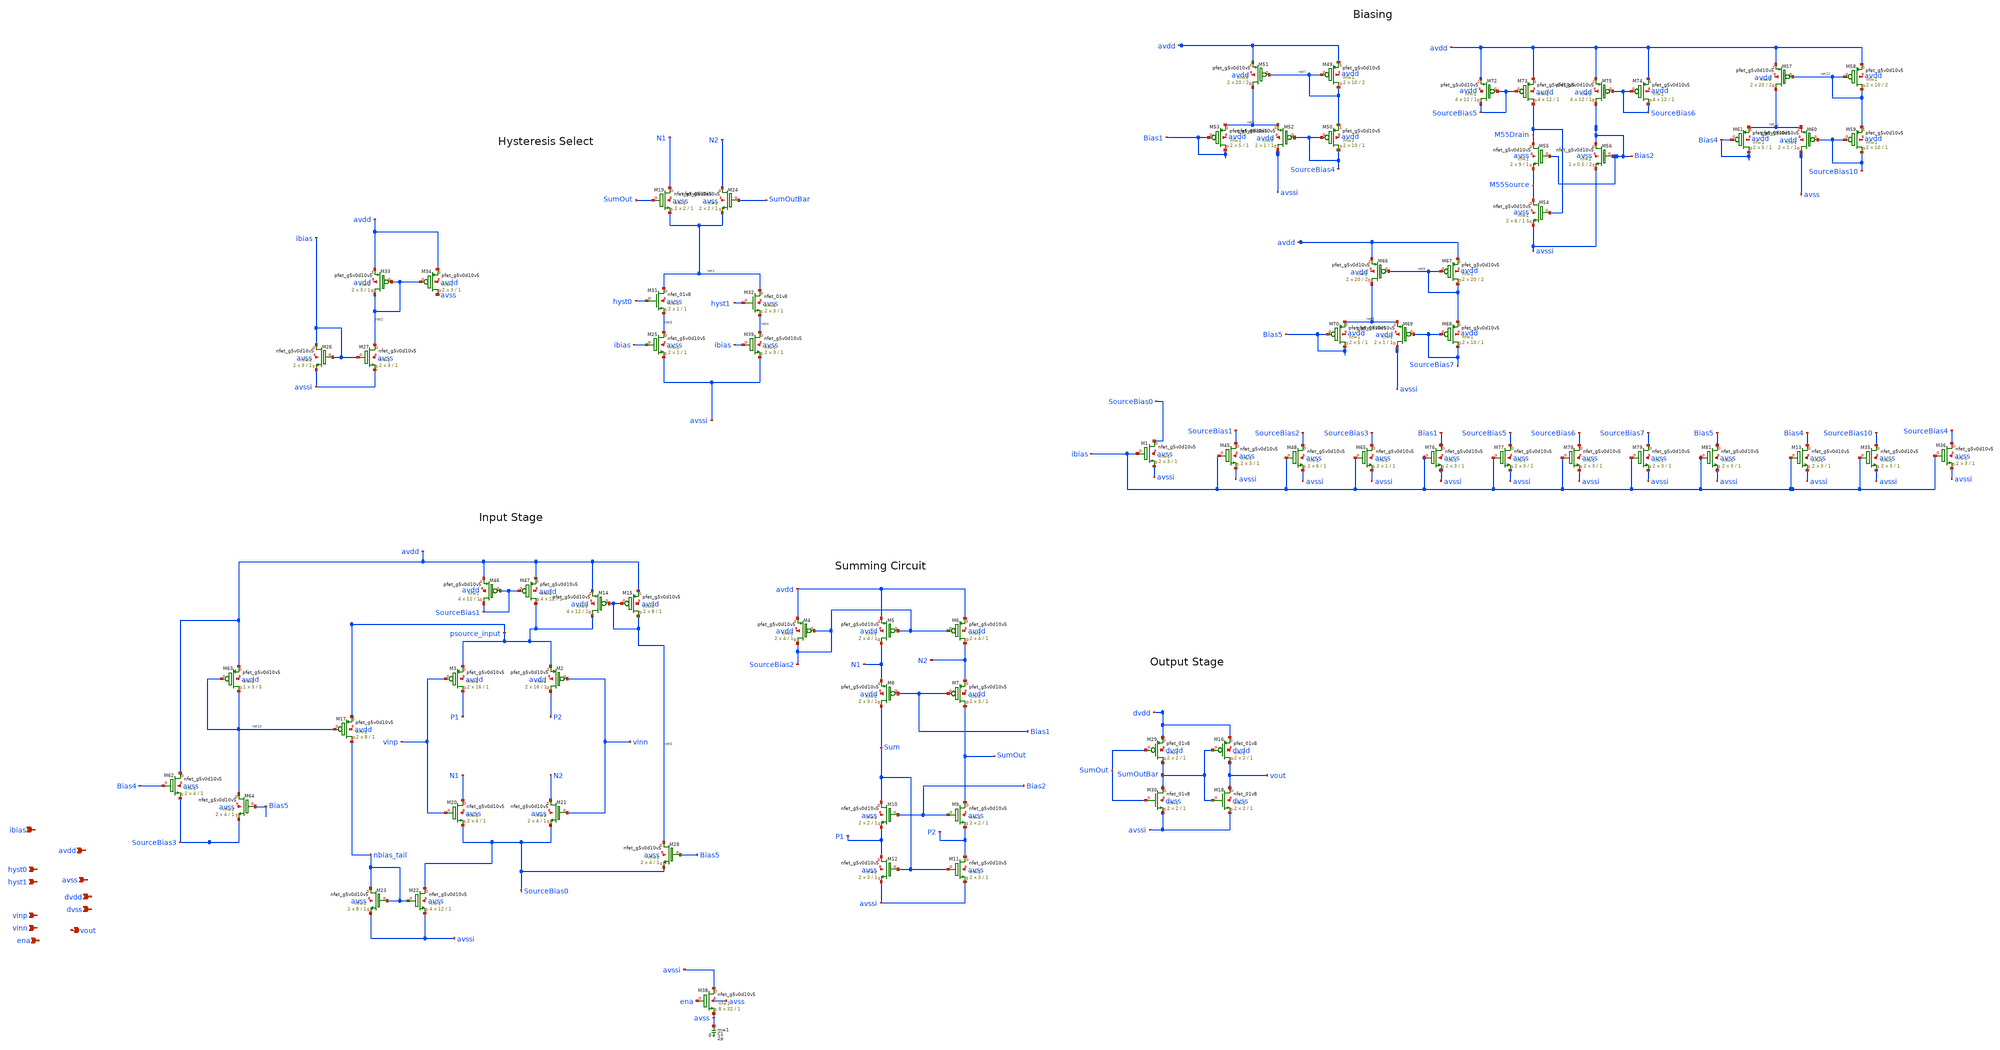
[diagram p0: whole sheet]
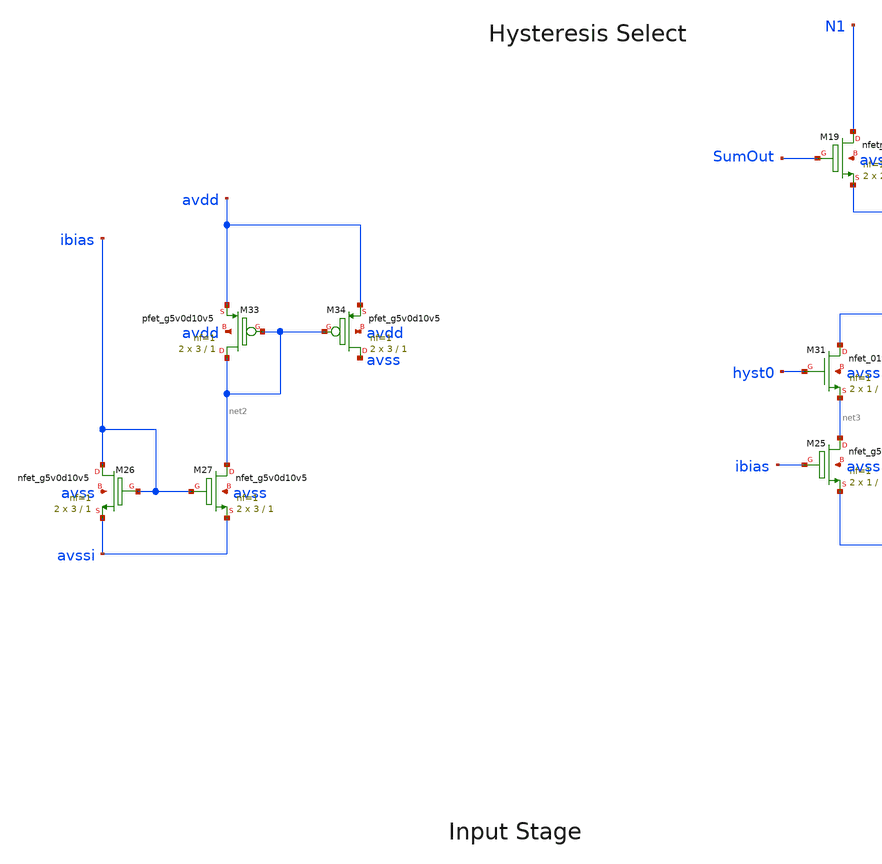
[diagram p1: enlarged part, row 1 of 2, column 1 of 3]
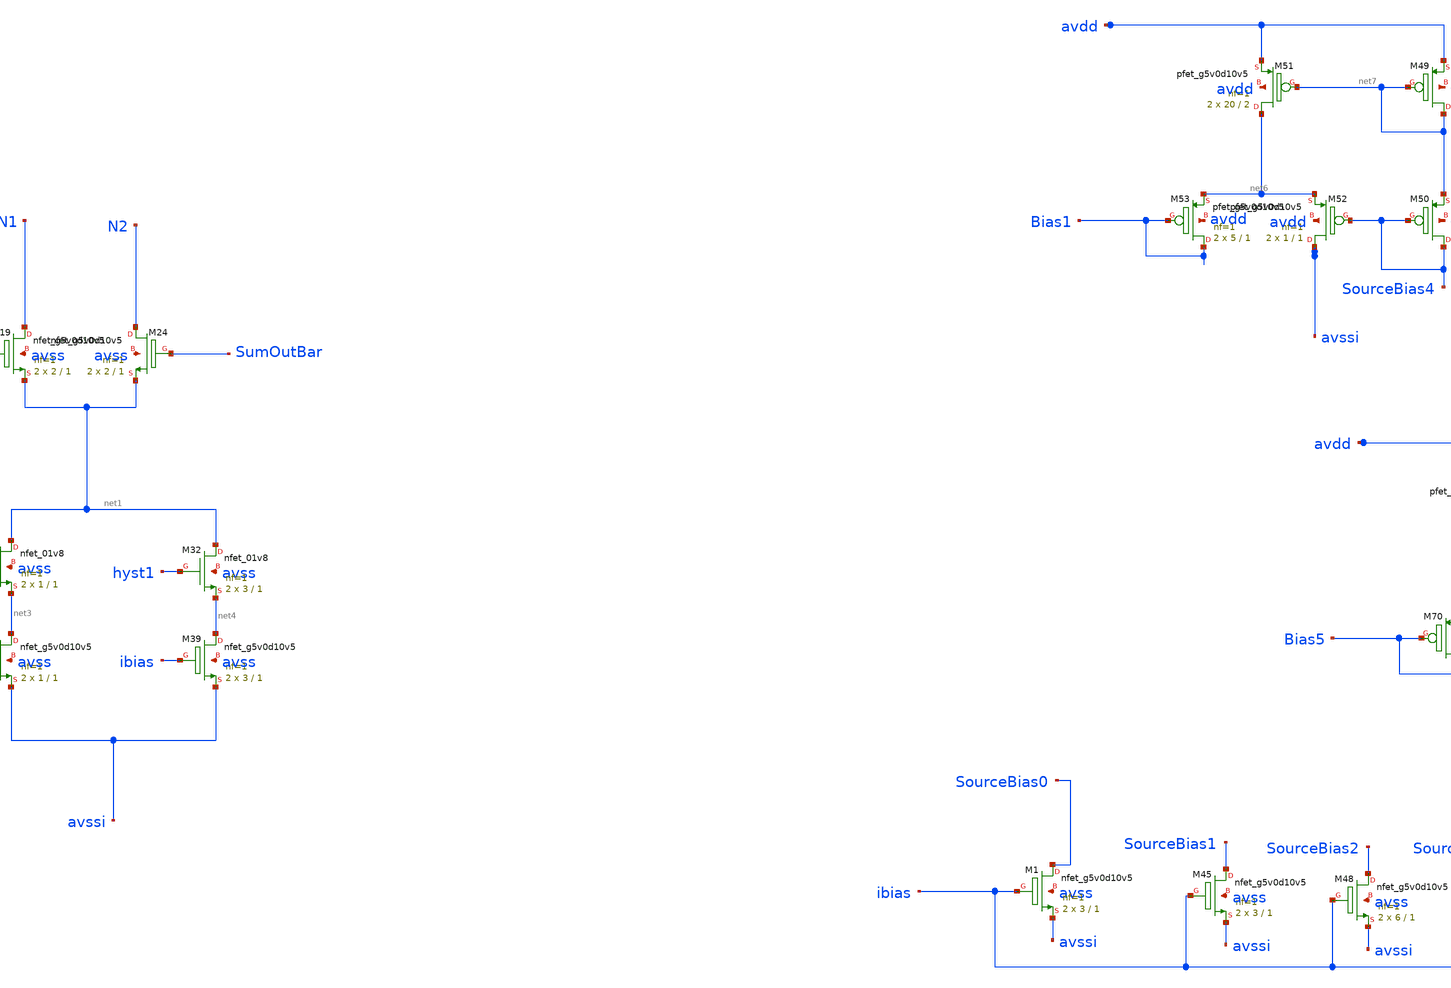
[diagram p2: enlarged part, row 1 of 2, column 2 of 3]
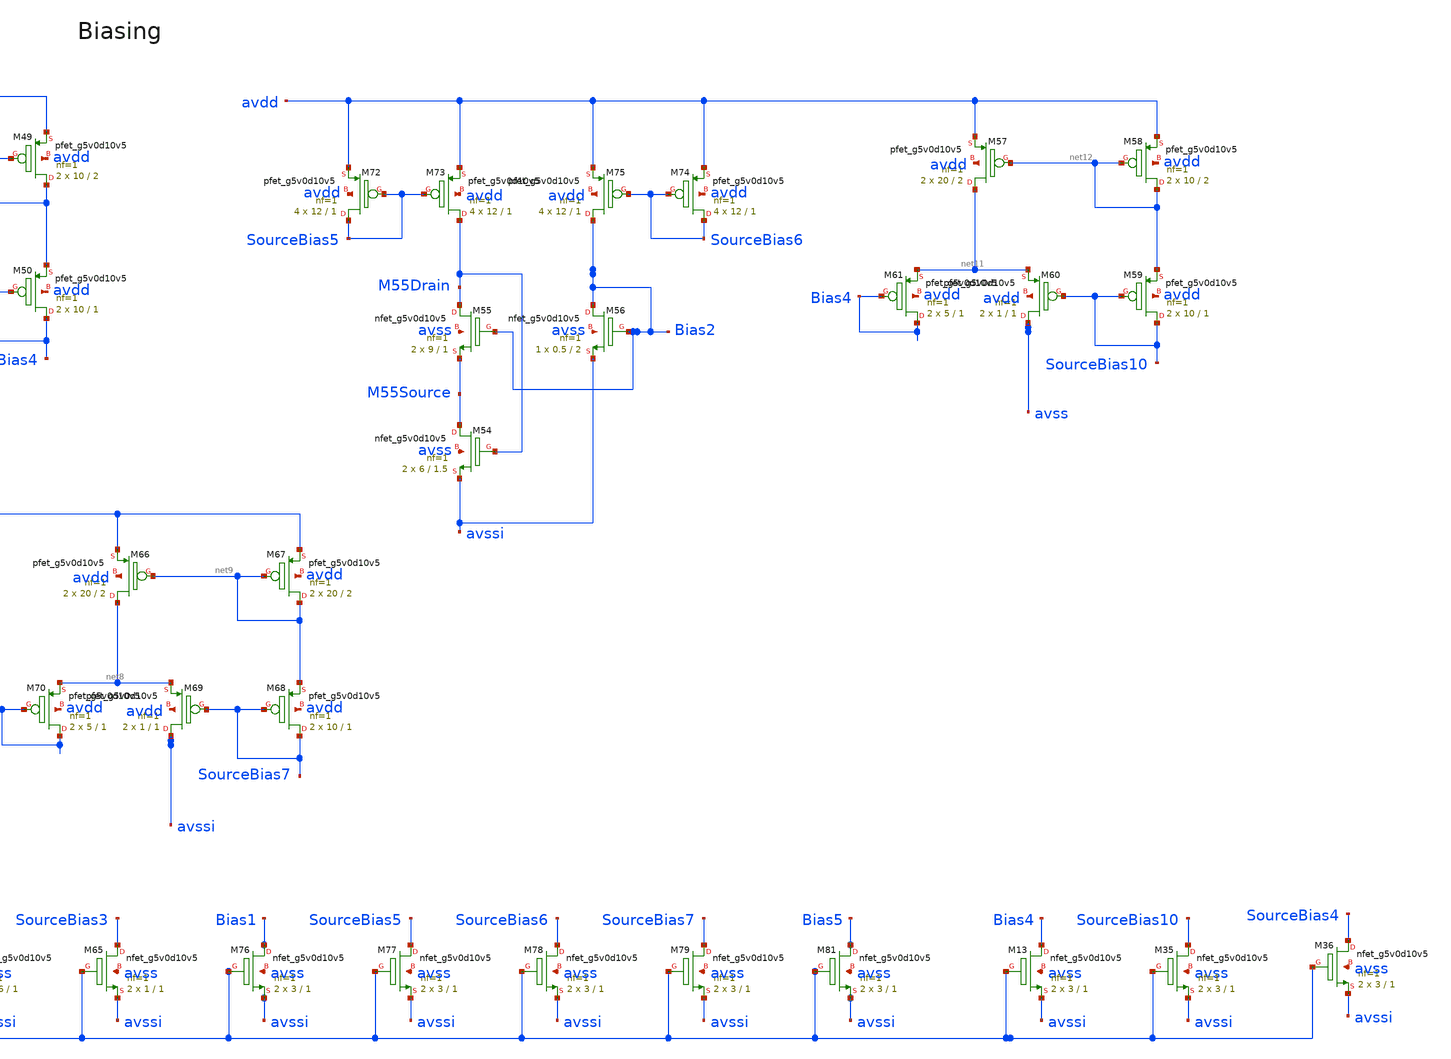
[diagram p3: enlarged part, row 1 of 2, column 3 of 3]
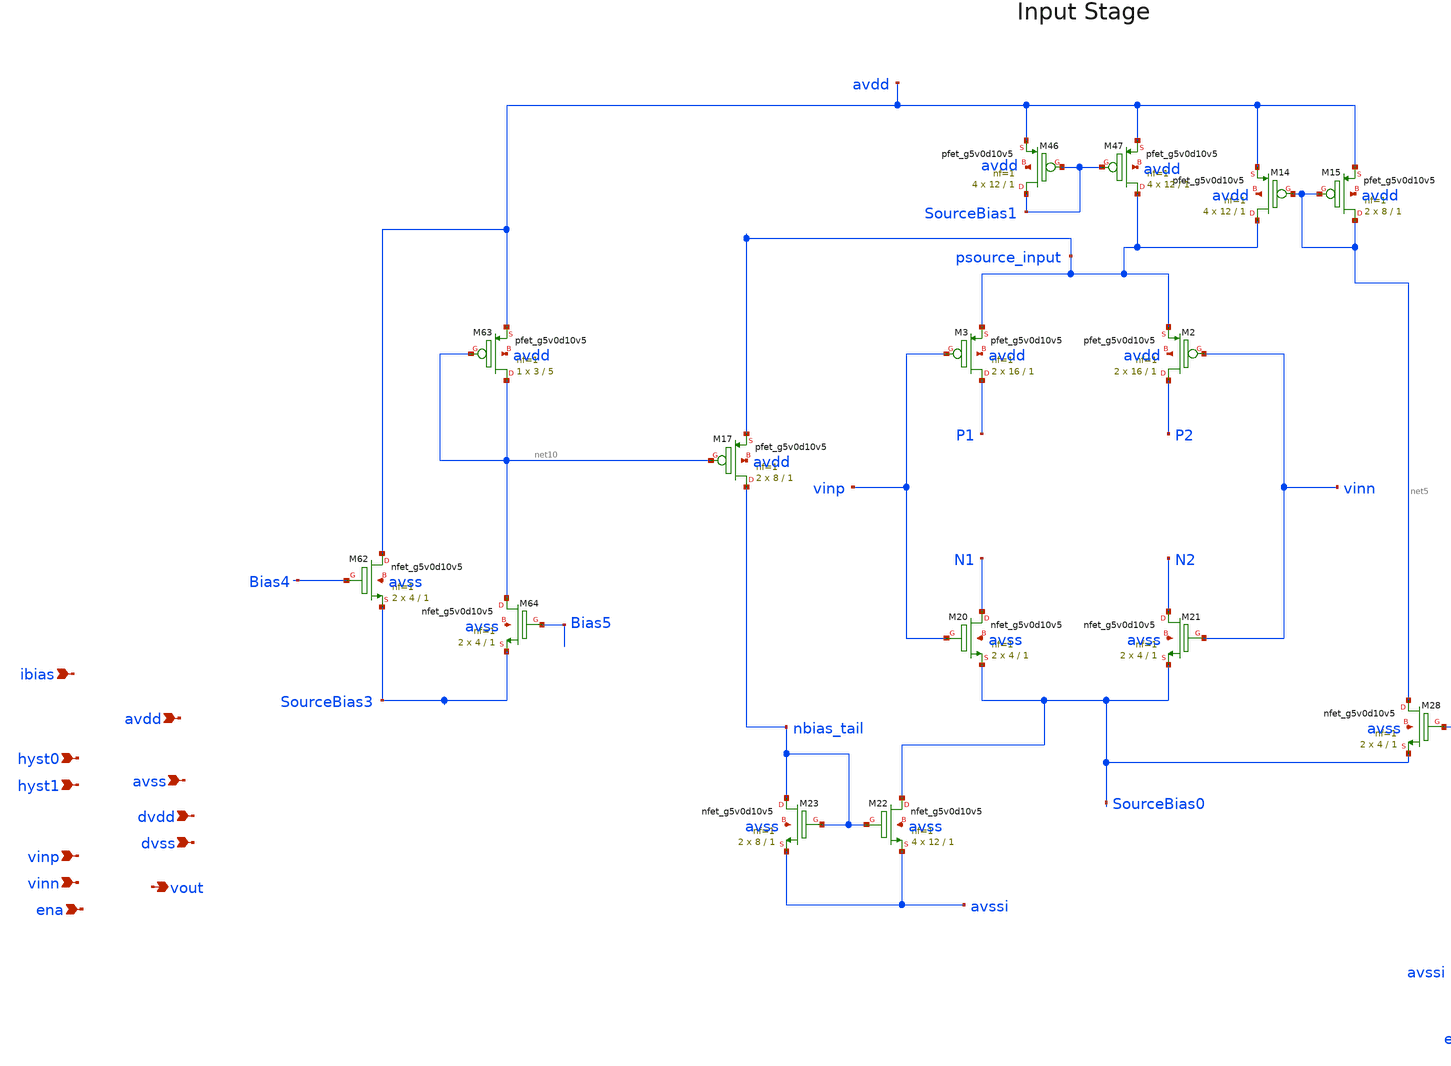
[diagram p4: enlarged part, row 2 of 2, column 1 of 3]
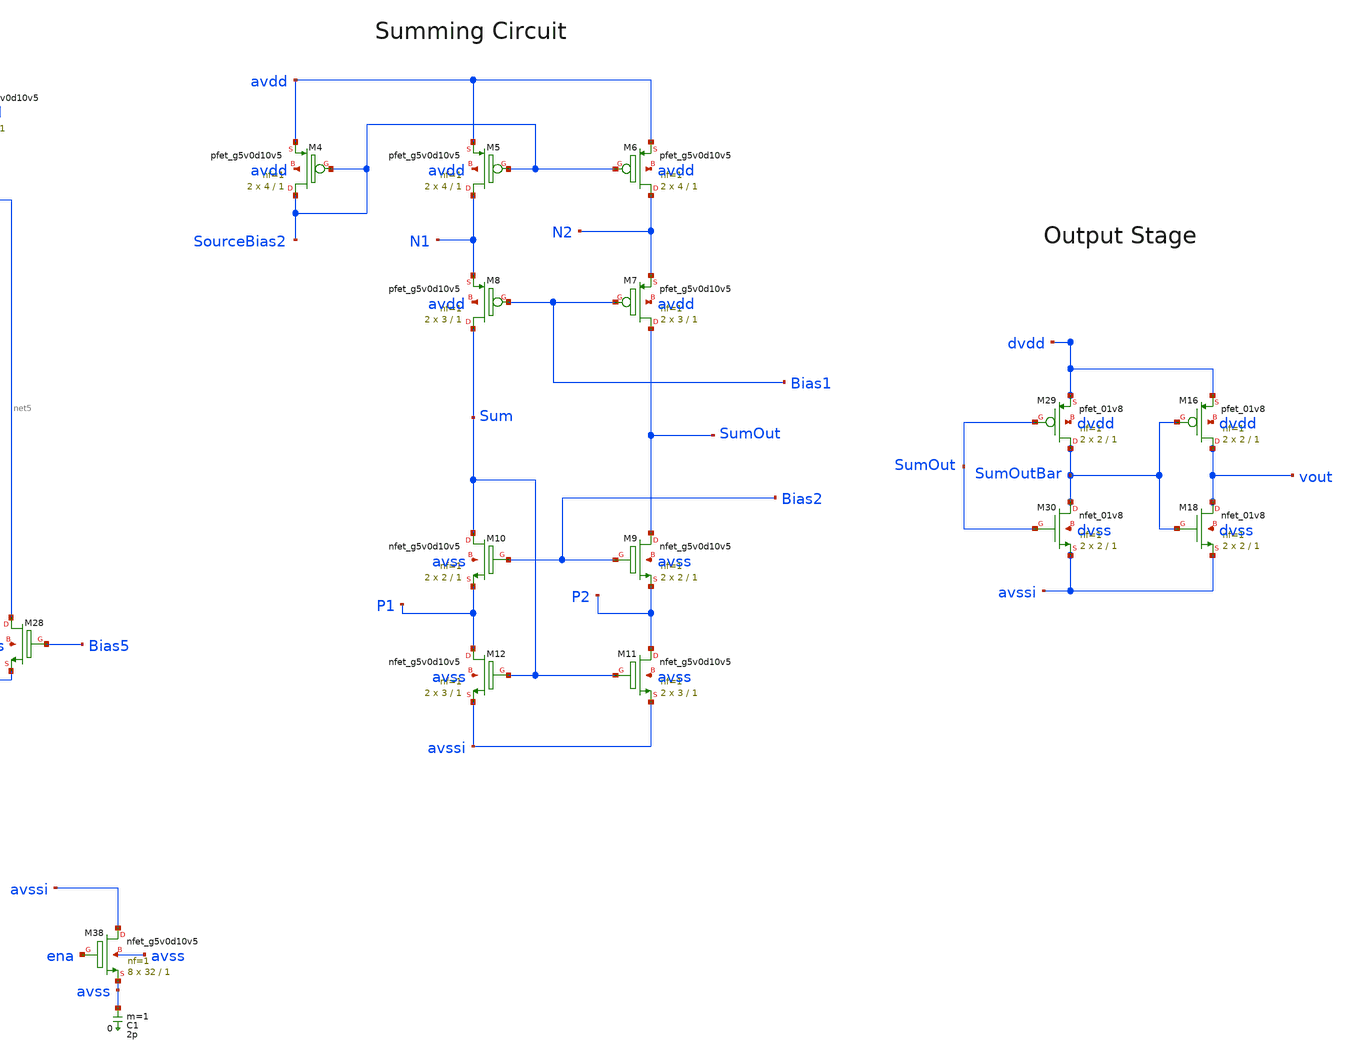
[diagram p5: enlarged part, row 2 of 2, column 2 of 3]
** sch_path: Chipalooza_April2024_Comparator/xschem/Chipalooza_April2024_Comparator(copy5).sch
**.subckt Chipalooza_April2024_Comparator(copy5) vinp vinn hyst0 hyst1 avdd avss dvdd dvss vout ena
*+ ibias
*.ipin vinp
*.ipin vinn
*.ipin hyst0
*.ipin hyst1
*.ipin avdd
*.ipin avss
*.ipin dvdd
*.ipin dvss
*.opin vout
*.ipin ena
*.ipin ibias
XM29 SumOutBar SumOut dvdd dvdd sky130_fd_pr__pfet_01v8 L=1 W=2 nf=1 ad='int((nf+1)/2) * W/nf * 0.29'
+ as='int((nf+2)/2) * W/nf * 0.29' pd='2*int((nf+1)/2) * (W/nf + 0.29)' ps='2*int((nf+2)/2) * (W/nf + 0.29)'
+ nrd='0.29 / W' nrs='0.29 / W' sa=0 sb=0 sd=0 mult=2 m=2
XM30 SumOutBar SumOut avssi dvss sky130_fd_pr__nfet_01v8 L=1 W=2 nf=1 ad='int((nf+1)/2) * W/nf * 0.29'
+ as='int((nf+2)/2) * W/nf * 0.29' pd='2*int((nf+1)/2) * (W/nf + 0.29)' ps='2*int((nf+2)/2) * (W/nf + 0.29)'
+ nrd='0.29 / W' nrs='0.29 / W' sa=0 sb=0 sd=0 mult=2 m=2
XM25 net3 ibias avssi avss sky130_fd_pr__nfet_g5v0d10v5 L=1 W=1 nf=1 ad='int((nf+1)/2) * W/nf * 0.29'
+ as='int((nf+2)/2) * W/nf * 0.29' pd='2*int((nf+1)/2) * (W/nf + 0.29)' ps='2*int((nf+2)/2) * (W/nf + 0.29)'
+ nrd='0.29 / W' nrs='0.29 / W' sa=0 sb=0 sd=0 mult=2 m=2
C1 avss 0 2p m=1
XM38 avssi ena avss avss sky130_fd_pr__nfet_g5v0d10v5 L=1 W=32 nf=1 ad='int((nf+1)/2) * W/nf * 0.29'
+ as='int((nf+2)/2) * W/nf * 0.29' pd='2*int((nf+1)/2) * (W/nf + 0.29)' ps='2*int((nf+2)/2) * (W/nf + 0.29)'
+ nrd='0.29 / W' nrs='0.29 / W' sa=0 sb=0 sd=0 mult=8 m=8
XM39 net4 ibias avssi avss sky130_fd_pr__nfet_g5v0d10v5 L=1 W=3 nf=1 ad='int((nf+1)/2) * W/nf * 0.29'
+ as='int((nf+2)/2) * W/nf * 0.29' pd='2*int((nf+1)/2) * (W/nf + 0.29)' ps='2*int((nf+2)/2) * (W/nf + 0.29)'
+ nrd='0.29 / W' nrs='0.29 / W' sa=0 sb=0 sd=0 mult=2 m=2
XM16 vout SumOutBar dvdd dvdd sky130_fd_pr__pfet_01v8 L=1 W=2 nf=1 ad='int((nf+1)/2) * W/nf * 0.29' as='int((nf+2)/2) * W/nf * 0.29'
+ pd='2*int((nf+1)/2) * (W/nf + 0.29)' ps='2*int((nf+2)/2) * (W/nf + 0.29)' nrd='0.29 / W' nrs='0.29 / W'
+ sa=0 sb=0 sd=0 mult=2 m=2
XM18 vout SumOutBar avssi dvss sky130_fd_pr__nfet_01v8 L=1 W=2 nf=1 ad='int((nf+1)/2) * W/nf * 0.29'
+ as='int((nf+2)/2) * W/nf * 0.29' pd='2*int((nf+1)/2) * (W/nf + 0.29)' ps='2*int((nf+2)/2) * (W/nf + 0.29)'
+ nrd='0.29 / W' nrs='0.29 / W' sa=0 sb=0 sd=0 mult=2 m=2
XM4 SourceBias2 SourceBias2 avdd avdd sky130_fd_pr__pfet_g5v0d10v5 L=1 W=4 nf=1 ad='int((nf+1)/2) * W/nf * 0.29'
+ as='int((nf+2)/2) * W/nf * 0.29' pd='2*int((nf+1)/2) * (W/nf + 0.29)' ps='2*int((nf+2)/2) * (W/nf + 0.29)'
+ nrd='0.29 / W' nrs='0.29 / W' sa=0 sb=0 sd=0 mult=2 m=2
XM5 N1 SourceBias2 avdd avdd sky130_fd_pr__pfet_g5v0d10v5 L=1 W=4 nf=1 ad='int((nf+1)/2) * W/nf * 0.29'
+ as='int((nf+2)/2) * W/nf * 0.29' pd='2*int((nf+1)/2) * (W/nf + 0.29)' ps='2*int((nf+2)/2) * (W/nf + 0.29)'
+ nrd='0.29 / W' nrs='0.29 / W' sa=0 sb=0 sd=0 mult=2 m=2
XM6 N2 SourceBias2 avdd avdd sky130_fd_pr__pfet_g5v0d10v5 L=1 W=4 nf=1 ad='int((nf+1)/2) * W/nf * 0.29'
+ as='int((nf+2)/2) * W/nf * 0.29' pd='2*int((nf+1)/2) * (W/nf + 0.29)' ps='2*int((nf+2)/2) * (W/nf + 0.29)'
+ nrd='0.29 / W' nrs='0.29 / W' sa=0 sb=0 sd=0 mult=2 m=2
XM7 SumOut Bias1 N2 avdd sky130_fd_pr__pfet_g5v0d10v5 L=1 W=3 nf=1 ad='int((nf+1)/2) * W/nf * 0.29' as='int((nf+2)/2) * W/nf * 0.29'
+ pd='2*int((nf+1)/2) * (W/nf + 0.29)' ps='2*int((nf+2)/2) * (W/nf + 0.29)' nrd='0.29 / W' nrs='0.29 / W'
+ sa=0 sb=0 sd=0 mult=2 m=2
XM8 Sum Bias1 N1 avdd sky130_fd_pr__pfet_g5v0d10v5 L=1 W=3 nf=1 ad='int((nf+1)/2) * W/nf * 0.29' as='int((nf+2)/2) * W/nf * 0.29'
+ pd='2*int((nf+1)/2) * (W/nf + 0.29)' ps='2*int((nf+2)/2) * (W/nf + 0.29)' nrd='0.29 / W' nrs='0.29 / W'
+ sa=0 sb=0 sd=0 mult=2 m=2
XM9 SumOut Bias2 P2 avss sky130_fd_pr__nfet_g5v0d10v5 L=1 W=2 nf=1 ad='int((nf+1)/2) * W/nf * 0.29' as='int((nf+2)/2) * W/nf * 0.29'
+ pd='2*int((nf+1)/2) * (W/nf + 0.29)' ps='2*int((nf+2)/2) * (W/nf + 0.29)' nrd='0.29 / W' nrs='0.29 / W'
+ sa=0 sb=0 sd=0 mult=2 m=2
XM10 Sum Bias2 P1 avss sky130_fd_pr__nfet_g5v0d10v5 L=1 W=2 nf=1 ad='int((nf+1)/2) * W/nf * 0.29' as='int((nf+2)/2) * W/nf * 0.29'
+ pd='2*int((nf+1)/2) * (W/nf + 0.29)' ps='2*int((nf+2)/2) * (W/nf + 0.29)' nrd='0.29 / W' nrs='0.29 / W'
+ sa=0 sb=0 sd=0 mult=2 m=2
XM11 P2 Sum avssi avss sky130_fd_pr__nfet_g5v0d10v5 L=1 W=3 nf=1 ad='int((nf+1)/2) * W/nf * 0.29' as='int((nf+2)/2) * W/nf * 0.29'
+ pd='2*int((nf+1)/2) * (W/nf + 0.29)' ps='2*int((nf+2)/2) * (W/nf + 0.29)' nrd='0.29 / W' nrs='0.29 / W'
+ sa=0 sb=0 sd=0 mult=2 m=2
XM12 P1 Sum avssi avss sky130_fd_pr__nfet_g5v0d10v5 L=1 W=3 nf=1 ad='int((nf+1)/2) * W/nf * 0.29' as='int((nf+2)/2) * W/nf * 0.29'
+ pd='2*int((nf+1)/2) * (W/nf + 0.29)' ps='2*int((nf+2)/2) * (W/nf + 0.29)' nrd='0.29 / W' nrs='0.29 / W'
+ sa=0 sb=0 sd=0 mult=2 m=2
XM2 P2 vinn psource_input avdd sky130_fd_pr__pfet_g5v0d10v5 L=1 W=16 nf=1 ad='int((nf+1)/2) * W/nf * 0.29'
+ as='int((nf+2)/2) * W/nf * 0.29' pd='2*int((nf+1)/2) * (W/nf + 0.29)' ps='2*int((nf+2)/2) * (W/nf + 0.29)'
+ nrd='0.29 / W' nrs='0.29 / W' sa=0 sb=0 sd=0 mult=2 m=2
XM3 P1 vinp psource_input avdd sky130_fd_pr__pfet_g5v0d10v5 L=1 W=16 nf=1 ad='int((nf+1)/2) * W/nf * 0.29'
+ as='int((nf+2)/2) * W/nf * 0.29' pd='2*int((nf+1)/2) * (W/nf + 0.29)' ps='2*int((nf+2)/2) * (W/nf + 0.29)'
+ nrd='0.29 / W' nrs='0.29 / W' sa=0 sb=0 sd=0 mult=2 m=2
XM14 psource_input net5 avdd avdd sky130_fd_pr__pfet_g5v0d10v5 L=1 W=12 nf=1 ad='int((nf+1)/2) * W/nf * 0.29'
+ as='int((nf+2)/2) * W/nf * 0.29' pd='2*int((nf+1)/2) * (W/nf + 0.29)' ps='2*int((nf+2)/2) * (W/nf + 0.29)'
+ nrd='0.29 / W' nrs='0.29 / W' sa=0 sb=0 sd=0 mult=4 m=4
XM15 net5 net5 avdd avdd sky130_fd_pr__pfet_g5v0d10v5 L=1 W=8 nf=1 ad='int((nf+1)/2) * W/nf * 0.29' as='int((nf+2)/2) * W/nf * 0.29'
+ pd='2*int((nf+1)/2) * (W/nf + 0.29)' ps='2*int((nf+2)/2) * (W/nf + 0.29)' nrd='0.29 / W' nrs='0.29 / W'
+ sa=0 sb=0 sd=0 mult=2 m=2
XM17 nbias_tail net10 psource_input avdd sky130_fd_pr__pfet_g5v0d10v5 L=1 W=8 nf=1 ad='int((nf+1)/2) * W/nf * 0.29'
+ as='int((nf+2)/2) * W/nf * 0.29' pd='2*int((nf+1)/2) * (W/nf + 0.29)' ps='2*int((nf+2)/2) * (W/nf + 0.29)'
+ nrd='0.29 / W' nrs='0.29 / W' sa=0 sb=0 sd=0 mult=2 m=2
XM20 N1 vinp SourceBias0 avss sky130_fd_pr__nfet_g5v0d10v5 L=1 W=4 nf=1 ad='int((nf+1)/2) * W/nf * 0.29'
+ as='int((nf+2)/2) * W/nf * 0.29' pd='2*int((nf+1)/2) * (W/nf + 0.29)' ps='2*int((nf+2)/2) * (W/nf + 0.29)'
+ nrd='0.29 / W' nrs='0.29 / W' sa=0 sb=0 sd=0 mult=2 m=2
XM21 N2 vinn SourceBias0 avss sky130_fd_pr__nfet_g5v0d10v5 L=1 W=4 nf=1 ad='int((nf+1)/2) * W/nf * 0.29'
+ as='int((nf+2)/2) * W/nf * 0.29' pd='2*int((nf+1)/2) * (W/nf + 0.29)' ps='2*int((nf+2)/2) * (W/nf + 0.29)'
+ nrd='0.29 / W' nrs='0.29 / W' sa=0 sb=0 sd=0 mult=2 m=2
XM22 SourceBias0 nbias_tail avssi avss sky130_fd_pr__nfet_g5v0d10v5 L=1 W=12 nf=1 ad='int((nf+1)/2) * W/nf * 0.29'
+ as='int((nf+2)/2) * W/nf * 0.29' pd='2*int((nf+1)/2) * (W/nf + 0.29)' ps='2*int((nf+2)/2) * (W/nf + 0.29)'
+ nrd='0.29 / W' nrs='0.29 / W' sa=0 sb=0 sd=0 mult=4 m=4
XM23 nbias_tail nbias_tail avssi avss sky130_fd_pr__nfet_g5v0d10v5 L=1 W=8 nf=1 ad='int((nf+1)/2) * W/nf * 0.29'
+ as='int((nf+2)/2) * W/nf * 0.29' pd='2*int((nf+1)/2) * (W/nf + 0.29)' ps='2*int((nf+2)/2) * (W/nf + 0.29)'
+ nrd='0.29 / W' nrs='0.29 / W' sa=0 sb=0 sd=0 mult=2 m=2
XM28 net5 Bias5 SourceBias0 avss sky130_fd_pr__nfet_g5v0d10v5 L=1 W=4 nf=1 ad='int((nf+1)/2) * W/nf * 0.29'
+ as='int((nf+2)/2) * W/nf * 0.29' pd='2*int((nf+1)/2) * (W/nf + 0.29)' ps='2*int((nf+2)/2) * (W/nf + 0.29)'
+ nrd='0.29 / W' nrs='0.29 / W' sa=0 sb=0 sd=0 mult=2 m=2
XM45 SourceBias1 ibias avssi avss sky130_fd_pr__nfet_g5v0d10v5 L=1 W=3 nf=1 ad='int((nf+1)/2) * W/nf * 0.29'
+ as='int((nf+2)/2) * W/nf * 0.29' pd='2*int((nf+1)/2) * (W/nf + 0.29)' ps='2*int((nf+2)/2) * (W/nf + 0.29)'
+ nrd='0.29 / W' nrs='0.29 / W' sa=0 sb=0 sd=0 mult=2 m=2
XM46 SourceBias1 SourceBias1 avdd avdd sky130_fd_pr__pfet_g5v0d10v5 L=1 W=12 nf=1 ad='int((nf+1)/2) * W/nf * 0.29'
+ as='int((nf+2)/2) * W/nf * 0.29' pd='2*int((nf+1)/2) * (W/nf + 0.29)' ps='2*int((nf+2)/2) * (W/nf + 0.29)'
+ nrd='0.29 / W' nrs='0.29 / W' sa=0 sb=0 sd=0 mult=4 m=4
XM47 psource_input SourceBias1 avdd avdd sky130_fd_pr__pfet_g5v0d10v5 L=1 W=12 nf=1 ad='int((nf+1)/2) * W/nf * 0.29'
+ as='int((nf+2)/2) * W/nf * 0.29' pd='2*int((nf+1)/2) * (W/nf + 0.29)' ps='2*int((nf+2)/2) * (W/nf + 0.29)'
+ nrd='0.29 / W' nrs='0.29 / W' sa=0 sb=0 sd=0 mult=4 m=4
XM48 SourceBias2 ibias avssi avss sky130_fd_pr__nfet_g5v0d10v5 L=1 W=6 nf=1 ad='int((nf+1)/2) * W/nf * 0.29'
+ as='int((nf+2)/2) * W/nf * 0.29' pd='2*int((nf+1)/2) * (W/nf + 0.29)' ps='2*int((nf+2)/2) * (W/nf + 0.29)'
+ nrd='0.29 / W' nrs='0.29 / W' sa=0 sb=0 sd=0 mult=2 m=2
XM65 SourceBias3 ibias avssi avss sky130_fd_pr__nfet_g5v0d10v5 L=1 W=1 nf=1 ad='int((nf+1)/2) * W/nf * 0.29'
+ as='int((nf+2)/2) * W/nf * 0.29' pd='2*int((nf+1)/2) * (W/nf + 0.29)' ps='2*int((nf+2)/2) * (W/nf + 0.29)'
+ nrd='0.29 / W' nrs='0.29 / W' sa=0 sb=0 sd=0 mult=2 m=2
XM76 Bias1 ibias avssi avss sky130_fd_pr__nfet_g5v0d10v5 L=1 W=3 nf=1 ad='int((nf+1)/2) * W/nf * 0.29'
+ as='int((nf+2)/2) * W/nf * 0.29' pd='2*int((nf+1)/2) * (W/nf + 0.29)' ps='2*int((nf+2)/2) * (W/nf + 0.29)'
+ nrd='0.29 / W' nrs='0.29 / W' sa=0 sb=0 sd=0 mult=2 m=2
XM77 SourceBias5 ibias avssi avss sky130_fd_pr__nfet_g5v0d10v5 L=1 W=3 nf=1 ad='int((nf+1)/2) * W/nf * 0.29'
+ as='int((nf+2)/2) * W/nf * 0.29' pd='2*int((nf+1)/2) * (W/nf + 0.29)' ps='2*int((nf+2)/2) * (W/nf + 0.29)'
+ nrd='0.29 / W' nrs='0.29 / W' sa=0 sb=0 sd=0 mult=2 m=2
XM78 SourceBias6 ibias avssi avss sky130_fd_pr__nfet_g5v0d10v5 L=1 W=3 nf=1 ad='int((nf+1)/2) * W/nf * 0.29'
+ as='int((nf+2)/2) * W/nf * 0.29' pd='2*int((nf+1)/2) * (W/nf + 0.29)' ps='2*int((nf+2)/2) * (W/nf + 0.29)'
+ nrd='0.29 / W' nrs='0.29 / W' sa=0 sb=0 sd=0 mult=2 m=2
XM79 SourceBias7 ibias avssi avss sky130_fd_pr__nfet_g5v0d10v5 L=1 W=3 nf=1 ad='int((nf+1)/2) * W/nf * 0.29'
+ as='int((nf+2)/2) * W/nf * 0.29' pd='2*int((nf+1)/2) * (W/nf + 0.29)' ps='2*int((nf+2)/2) * (W/nf + 0.29)'
+ nrd='0.29 / W' nrs='0.29 / W' sa=0 sb=0 sd=0 mult=2 m=2
XM81 Bias5 ibias avssi avss sky130_fd_pr__nfet_g5v0d10v5 L=1 W=3 nf=1 ad='int((nf+1)/2) * W/nf * 0.29'
+ as='int((nf+2)/2) * W/nf * 0.29' pd='2*int((nf+1)/2) * (W/nf + 0.29)' ps='2*int((nf+2)/2) * (W/nf + 0.29)'
+ nrd='0.29 / W' nrs='0.29 / W' sa=0 sb=0 sd=0 mult=2 m=2
XM54 M55Source M55Drain avssi avss sky130_fd_pr__nfet_g5v0d10v5 L=1.5 W=6 nf=1 ad='int((nf+1)/2) * W/nf * 0.29'
+ as='int((nf+2)/2) * W/nf * 0.29' pd='2*int((nf+1)/2) * (W/nf + 0.29)' ps='2*int((nf+2)/2) * (W/nf + 0.29)'
+ nrd='0.29 / W' nrs='0.29 / W' sa=0 sb=0 sd=0 mult=2 m=2
XM55 M55Drain Bias2 M55Source avss sky130_fd_pr__nfet_g5v0d10v5 L=1 W=9 nf=1 ad='int((nf+1)/2) * W/nf * 0.29'
+ as='int((nf+2)/2) * W/nf * 0.29' pd='2*int((nf+1)/2) * (W/nf + 0.29)' ps='2*int((nf+2)/2) * (W/nf + 0.29)'
+ nrd='0.29 / W' nrs='0.29 / W' sa=0 sb=0 sd=0 mult=2 m=2
XM56 Bias2 Bias2 avssi avss sky130_fd_pr__nfet_g5v0d10v5 L=2 W=0.5 nf=1 ad='int((nf+1)/2) * W/nf * 0.29'
+ as='int((nf+2)/2) * W/nf * 0.29' pd='2*int((nf+1)/2) * (W/nf + 0.29)' ps='2*int((nf+2)/2) * (W/nf + 0.29)'
+ nrd='0.29 / W' nrs='0.29 / W' sa=0 sb=0 sd=0 mult=1 m=1
XM51 net6 net7 avdd avdd sky130_fd_pr__pfet_g5v0d10v5 L=2 W=20 nf=1 ad='int((nf+1)/2) * W/nf * 0.29'
+ as='int((nf+2)/2) * W/nf * 0.29' pd='2*int((nf+1)/2) * (W/nf + 0.29)' ps='2*int((nf+2)/2) * (W/nf + 0.29)'
+ nrd='0.29 / W' nrs='0.29 / W' sa=0 sb=0 sd=0 mult=2 m=2
XM49 net7 net7 avdd avdd sky130_fd_pr__pfet_g5v0d10v5 L=2 W=10 nf=1 ad='int((nf+1)/2) * W/nf * 0.29'
+ as='int((nf+2)/2) * W/nf * 0.29' pd='2*int((nf+1)/2) * (W/nf + 0.29)' ps='2*int((nf+2)/2) * (W/nf + 0.29)'
+ nrd='0.29 / W' nrs='0.29 / W' sa=0 sb=0 sd=0 mult=2 m=2
XM50 SourceBias4 SourceBias4 net7 avdd sky130_fd_pr__pfet_g5v0d10v5 L=1 W=10 nf=1 ad='int((nf+1)/2) * W/nf * 0.29'
+ as='int((nf+2)/2) * W/nf * 0.29' pd='2*int((nf+1)/2) * (W/nf + 0.29)' ps='2*int((nf+2)/2) * (W/nf + 0.29)'
+ nrd='0.29 / W' nrs='0.29 / W' sa=0 sb=0 sd=0 mult=2 m=2
XM52 avssi SourceBias4 net6 avdd sky130_fd_pr__pfet_g5v0d10v5 L=1 W=1 nf=1 ad='int((nf+1)/2) * W/nf * 0.29'
+ as='int((nf+2)/2) * W/nf * 0.29' pd='2*int((nf+1)/2) * (W/nf + 0.29)' ps='2*int((nf+2)/2) * (W/nf + 0.29)'
+ nrd='0.29 / W' nrs='0.29 / W' sa=0 sb=0 sd=0 mult=2 m=2
XM53 Bias1 Bias1 net6 avdd sky130_fd_pr__pfet_g5v0d10v5 L=1 W=5 nf=1 ad='int((nf+1)/2) * W/nf * 0.29'
+ as='int((nf+2)/2) * W/nf * 0.29' pd='2*int((nf+1)/2) * (W/nf + 0.29)' ps='2*int((nf+2)/2) * (W/nf + 0.29)'
+ nrd='0.29 / W' nrs='0.29 / W' sa=0 sb=0 sd=0 mult=2 m=2
XM66 net8 net9 avdd avdd sky130_fd_pr__pfet_g5v0d10v5 L=2 W=20 nf=1 ad='int((nf+1)/2) * W/nf * 0.29'
+ as='int((nf+2)/2) * W/nf * 0.29' pd='2*int((nf+1)/2) * (W/nf + 0.29)' ps='2*int((nf+2)/2) * (W/nf + 0.29)'
+ nrd='0.29 / W' nrs='0.29 / W' sa=0 sb=0 sd=0 mult=2 m=2
XM67 net9 net9 avdd avdd sky130_fd_pr__pfet_g5v0d10v5 L=2 W=20 nf=1 ad='int((nf+1)/2) * W/nf * 0.29'
+ as='int((nf+2)/2) * W/nf * 0.29' pd='2*int((nf+1)/2) * (W/nf + 0.29)' ps='2*int((nf+2)/2) * (W/nf + 0.29)'
+ nrd='0.29 / W' nrs='0.29 / W' sa=0 sb=0 sd=0 mult=2 m=2
XM68 SourceBias7 SourceBias7 net9 avdd sky130_fd_pr__pfet_g5v0d10v5 L=1 W=10 nf=1 ad='int((nf+1)/2) * W/nf * 0.29'
+ as='int((nf+2)/2) * W/nf * 0.29' pd='2*int((nf+1)/2) * (W/nf + 0.29)' ps='2*int((nf+2)/2) * (W/nf + 0.29)'
+ nrd='0.29 / W' nrs='0.29 / W' sa=0 sb=0 sd=0 mult=2 m=2
XM69 avssi SourceBias7 net8 avdd sky130_fd_pr__pfet_g5v0d10v5 L=1 W=1 nf=1 ad='int((nf+1)/2) * W/nf * 0.29'
+ as='int((nf+2)/2) * W/nf * 0.29' pd='2*int((nf+1)/2) * (W/nf + 0.29)' ps='2*int((nf+2)/2) * (W/nf + 0.29)'
+ nrd='0.29 / W' nrs='0.29 / W' sa=0 sb=0 sd=0 mult=2 m=2
XM70 Bias5 Bias5 net8 avdd sky130_fd_pr__pfet_g5v0d10v5 L=1 W=5 nf=1 ad='int((nf+1)/2) * W/nf * 0.29'
+ as='int((nf+2)/2) * W/nf * 0.29' pd='2*int((nf+1)/2) * (W/nf + 0.29)' ps='2*int((nf+2)/2) * (W/nf + 0.29)'
+ nrd='0.29 / W' nrs='0.29 / W' sa=0 sb=0 sd=0 mult=2 m=2
XM72 SourceBias5 SourceBias5 avdd avdd sky130_fd_pr__pfet_g5v0d10v5 L=1 W=12 nf=1 ad='int((nf+1)/2) * W/nf * 0.29'
+ as='int((nf+2)/2) * W/nf * 0.29' pd='2*int((nf+1)/2) * (W/nf + 0.29)' ps='2*int((nf+2)/2) * (W/nf + 0.29)'
+ nrd='0.29 / W' nrs='0.29 / W' sa=0 sb=0 sd=0 mult=4 m=4
XM73 M55Drain SourceBias5 avdd avdd sky130_fd_pr__pfet_g5v0d10v5 L=1 W=12 nf=1 ad='int((nf+1)/2) * W/nf * 0.29'
+ as='int((nf+2)/2) * W/nf * 0.29' pd='2*int((nf+1)/2) * (W/nf + 0.29)' ps='2*int((nf+2)/2) * (W/nf + 0.29)'
+ nrd='0.29 / W' nrs='0.29 / W' sa=0 sb=0 sd=0 mult=4 m=4
XM74 SourceBias6 SourceBias6 avdd avdd sky130_fd_pr__pfet_g5v0d10v5 L=1 W=12 nf=1 ad='int((nf+1)/2) * W/nf * 0.29'
+ as='int((nf+2)/2) * W/nf * 0.29' pd='2*int((nf+1)/2) * (W/nf + 0.29)' ps='2*int((nf+2)/2) * (W/nf + 0.29)'
+ nrd='0.29 / W' nrs='0.29 / W' sa=0 sb=0 sd=0 mult=4 m=4
XM75 Bias2 SourceBias6 avdd avdd sky130_fd_pr__pfet_g5v0d10v5 L=1 W=12 nf=1 ad='int((nf+1)/2) * W/nf * 0.29'
+ as='int((nf+2)/2) * W/nf * 0.29' pd='2*int((nf+1)/2) * (W/nf + 0.29)' ps='2*int((nf+2)/2) * (W/nf + 0.29)'
+ nrd='0.29 / W' nrs='0.29 / W' sa=0 sb=0 sd=0 mult=4 m=4
XM1 SourceBias0 ibias avssi avss sky130_fd_pr__nfet_g5v0d10v5 L=1 W=3 nf=1 ad='int((nf+1)/2) * W/nf * 0.29'
+ as='int((nf+2)/2) * W/nf * 0.29' pd='2*int((nf+1)/2) * (W/nf + 0.29)' ps='2*int((nf+2)/2) * (W/nf + 0.29)'
+ nrd='0.29 / W' nrs='0.29 / W' sa=0 sb=0 sd=0 mult=2 m=2
XM31 net1 hyst0 net3 avss sky130_fd_pr__nfet_01v8 L=1 W=1 nf=1 ad='int((1 + 1)/2) * 1 / 1 * 0.29' as='int((1 + 2)/2) * 1 / 1 * 0.29'
+ pd='2*int((1 + 1)/2) * (1 / 1 + 0.29)' ps='2*int((1 + 2)/2) * (1 / 1 + 0.29)' nrd='0.29 / 1 ' nrs='0.29 / 1 '
+ sa=0 sb=0 sd=0 mult=2 m=2
XM32 net1 hyst1 net4 avss sky130_fd_pr__nfet_01v8 L=1 W=3 nf=1 ad='int((1 + 1)/2) * 3 / 1 * 0.29' as='int((1 + 2)/2) * 3 / 1 * 0.29'
+ pd='2*int((1 + 1)/2) * (3 / 1 + 0.29)' ps='2*int((1 + 2)/2) * (3 / 1 + 0.29)' nrd='0.29 / 3 ' nrs='0.29 / 3 '
+ sa=0 sb=0 sd=0 mult=2 m=2
XM19 N1 SumOut net1 avss sky130_fd_pr__nfet_g5v0d10v5 L=1 W=2 nf=1 ad='int((nf+1)/2) * W/nf * 0.29' as='int((nf+2)/2) * W/nf * 0.29'
+ pd='2*int((nf+1)/2) * (W/nf + 0.29)' ps='2*int((nf+2)/2) * (W/nf + 0.29)' nrd='0.29 / W' nrs='0.29 / W'
+ sa=0 sb=0 sd=0 mult=2 m=2
XM24 N2 SumOutBar net1 avss sky130_fd_pr__nfet_g5v0d10v5 L=1 W=2 nf=1 ad='int((nf+1)/2) * W/nf * 0.29'
+ as='int((nf+2)/2) * W/nf * 0.29' pd='2*int((nf+1)/2) * (W/nf + 0.29)' ps='2*int((nf+2)/2) * (W/nf + 0.29)'
+ nrd='0.29 / W' nrs='0.29 / W' sa=0 sb=0 sd=0 mult=2 m=2
XM26 ibias ibias avssi avss sky130_fd_pr__nfet_g5v0d10v5 L=1 W=3 nf=1 ad='int((nf+1)/2) * W/nf * 0.29'
+ as='int((nf+2)/2) * W/nf * 0.29' pd='2*int((nf+1)/2) * (W/nf + 0.29)' ps='2*int((nf+2)/2) * (W/nf + 0.29)'
+ nrd='0.29 / W' nrs='0.29 / W' sa=0 sb=0 sd=0 mult=2 m=2
XM27 net2 ibias avssi avss sky130_fd_pr__nfet_g5v0d10v5 L=1 W=3 nf=1 ad='int((nf+1)/2) * W/nf * 0.29'
+ as='int((nf+2)/2) * W/nf * 0.29' pd='2*int((nf+1)/2) * (W/nf + 0.29)' ps='2*int((nf+2)/2) * (W/nf + 0.29)'
+ nrd='0.29 / W' nrs='0.29 / W' sa=0 sb=0 sd=0 mult=2 m=2
XM33 net2 net2 avdd avdd sky130_fd_pr__pfet_g5v0d10v5 L=1 W=3 nf=1 ad='int((nf+1)/2) * W/nf * 0.29' as='int((nf+2)/2) * W/nf * 0.29'
+ pd='2*int((nf+1)/2) * (W/nf + 0.29)' ps='2*int((nf+2)/2) * (W/nf + 0.29)' nrd='0.29 / W' nrs='0.29 / W'
+ sa=0 sb=0 sd=0 mult=2 m=2
XM34 avss net2 avdd avdd sky130_fd_pr__pfet_g5v0d10v5 L=1 W=3 nf=1 ad='int((nf+1)/2) * W/nf * 0.29' as='int((nf+2)/2) * W/nf * 0.29'
+ pd='2*int((nf+1)/2) * (W/nf + 0.29)' ps='2*int((nf+2)/2) * (W/nf + 0.29)' nrd='0.29 / W' nrs='0.29 / W'
+ sa=0 sb=0 sd=0 mult=2 m=2
XM63 net10 net10 avdd avdd sky130_fd_pr__pfet_g5v0d10v5 L=5 W=3 nf=1 ad='int((nf+1)/2) * W/nf * 0.29'
+ as='int((nf+2)/2) * W/nf * 0.29' pd='2*int((nf+1)/2) * (W/nf + 0.29)' ps='2*int((nf+2)/2) * (W/nf + 0.29)'
+ nrd='0.29 / W' nrs='0.29 / W' sa=0 sb=0 sd=0 mult=1 m=1
XM62 avdd Bias4 SourceBias3 avss sky130_fd_pr__nfet_g5v0d10v5 L=1 W=4 nf=1 ad='int((nf+1)/2) * W/nf * 0.29'
+ as='int((nf+2)/2) * W/nf * 0.29' pd='2*int((nf+1)/2) * (W/nf + 0.29)' ps='2*int((nf+2)/2) * (W/nf + 0.29)'
+ nrd='0.29 / W' nrs='0.29 / W' sa=0 sb=0 sd=0 mult=2 m=2
XM64 net10 Bias5 SourceBias3 avss sky130_fd_pr__nfet_g5v0d10v5 L=1 W=4 nf=1 ad='int((nf+1)/2) * W/nf * 0.29'
+ as='int((nf+2)/2) * W/nf * 0.29' pd='2*int((nf+1)/2) * (W/nf + 0.29)' ps='2*int((nf+2)/2) * (W/nf + 0.29)'
+ nrd='0.29 / W' nrs='0.29 / W' sa=0 sb=0 sd=0 mult=2 m=2
XM57 net11 net12 avdd avdd sky130_fd_pr__pfet_g5v0d10v5 L=2 W=20 nf=1 ad='int((nf+1)/2) * W/nf * 0.29'
+ as='int((nf+2)/2) * W/nf * 0.29' pd='2*int((nf+1)/2) * (W/nf + 0.29)' ps='2*int((nf+2)/2) * (W/nf + 0.29)'
+ nrd='0.29 / W' nrs='0.29 / W' sa=0 sb=0 sd=0 mult=2 m=2
XM58 net12 net12 avdd avdd sky130_fd_pr__pfet_g5v0d10v5 L=2 W=10 nf=1 ad='int((nf+1)/2) * W/nf * 0.29'
+ as='int((nf+2)/2) * W/nf * 0.29' pd='2*int((nf+1)/2) * (W/nf + 0.29)' ps='2*int((nf+2)/2) * (W/nf + 0.29)'
+ nrd='0.29 / W' nrs='0.29 / W' sa=0 sb=0 sd=0 mult=2 m=2
XM59 SourceBias10 SourceBias10 net12 avdd sky130_fd_pr__pfet_g5v0d10v5 L=1 W=10 nf=1 ad='int((nf+1)/2) * W/nf * 0.29'
+ as='int((nf+2)/2) * W/nf * 0.29' pd='2*int((nf+1)/2) * (W/nf + 0.29)' ps='2*int((nf+2)/2) * (W/nf + 0.29)'
+ nrd='0.29 / W' nrs='0.29 / W' sa=0 sb=0 sd=0 mult=2 m=2
XM60 avss SourceBias10 net11 avdd sky130_fd_pr__pfet_g5v0d10v5 L=1 W=1 nf=1 ad='int((nf+1)/2) * W/nf * 0.29'
+ as='int((nf+2)/2) * W/nf * 0.29' pd='2*int((nf+1)/2) * (W/nf + 0.29)' ps='2*int((nf+2)/2) * (W/nf + 0.29)'
+ nrd='0.29 / W' nrs='0.29 / W' sa=0 sb=0 sd=0 mult=2 m=2
XM61 Bias4 Bias4 net11 avdd sky130_fd_pr__pfet_g5v0d10v5 L=1 W=5 nf=1 ad='int((nf+1)/2) * W/nf * 0.29'
+ as='int((nf+2)/2) * W/nf * 0.29' pd='2*int((nf+1)/2) * (W/nf + 0.29)' ps='2*int((nf+2)/2) * (W/nf + 0.29)'
+ nrd='0.29 / W' nrs='0.29 / W' sa=0 sb=0 sd=0 mult=2 m=2
XM13 Bias4 ibias avssi avss sky130_fd_pr__nfet_g5v0d10v5 L=1 W=3 nf=1 ad='int((nf+1)/2) * W/nf * 0.29'
+ as='int((nf+2)/2) * W/nf * 0.29' pd='2*int((nf+1)/2) * (W/nf + 0.29)' ps='2*int((nf+2)/2) * (W/nf + 0.29)'
+ nrd='0.29 / W' nrs='0.29 / W' sa=0 sb=0 sd=0 mult=2 m=2
XM35 SourceBias10 ibias avssi avss sky130_fd_pr__nfet_g5v0d10v5 L=1 W=3 nf=1 ad='int((nf+1)/2) * W/nf * 0.29'
+ as='int((nf+2)/2) * W/nf * 0.29' pd='2*int((nf+1)/2) * (W/nf + 0.29)' ps='2*int((nf+2)/2) * (W/nf + 0.29)'
+ nrd='0.29 / W' nrs='0.29 / W' sa=0 sb=0 sd=0 mult=2 m=2
XM36 SourceBias4 ibias avssi avss sky130_fd_pr__nfet_g5v0d10v5 L=1 W=3 nf=1 ad='int((nf+1)/2) * W/nf * 0.29'
+ as='int((nf+2)/2) * W/nf * 0.29' pd='2*int((nf+1)/2) * (W/nf + 0.29)' ps='2*int((nf+2)/2) * (W/nf + 0.29)'
+ nrd='0.29 / W' nrs='0.29 / W' sa=0 sb=0 sd=0 mult=2 m=2
**.ends
.end
